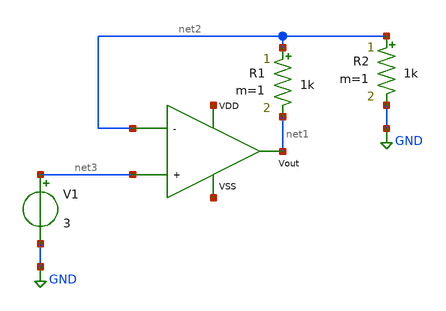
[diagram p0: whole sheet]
** sch_path: xschem/ota_miller/untitled.sch
**.subckt untitled
x1 net4 net1 net3 net2 net5 ota_n_in
V1 net3 GND 3
R1 net2 net1 1k m=1
R2 net2 GND 1k m=1
**.ends

* expanding   symbol:  ota_n_in.sym # of pins=5
** sym_path: xschem/ota_miller/ota_n_in.sym
** sch_path: xschem/ota_miller/ota_n_in.sch
.subckt ota_n_in VDD Vout + - VSS
*.opin Vout
*.ipin VSS
*.ipin VDD
*.ipin +
*.ipin -
XM1 net2 + net1 VSS nfet_03v3 L=0.28u W=0.22u nf=1 ad='int((nf+1)/2) * W/nf * 0.18u' as='int((nf+2)/2) * W/nf * 0.18u'
+ pd='2*int((nf+1)/2) * (W/nf + 0.18u)' ps='2*int((nf+2)/2) * (W/nf + 0.18u)' nrd='0.18u / W' nrs='0.18u / W'
+ sa=0 sb=0 sd=0 m=1 par=1
XM2 Vout - net1 VSS nfet_03v3 L=0.28u W=0.22u nf=1 ad='int((nf+1)/2) * W/nf * 0.18u' as='int((nf+2)/2) * W/nf * 0.18u'
+ pd='2*int((nf+1)/2) * (W/nf + 0.18u)' ps='2*int((nf+2)/2) * (W/nf + 0.18u)' nrd='0.18u / W' nrs='0.18u / W'
+ sa=0 sb=0 sd=0 m=1 par=1
XM3 VDD VDD net2 VSS nfet_03v3 L=0.28u W=0.22u nf=1 ad='int((nf+1)/2) * W/nf * 0.18u' as='int((nf+2)/2) * W/nf * 0.18u'
+ pd='2*int((nf+1)/2) * (W/nf + 0.18u)' ps='2*int((nf+2)/2) * (W/nf + 0.18u)' nrd='0.18u / W' nrs='0.18u / W'
+ sa=0 sb=0 sd=0 m=1 par=1
XM4 VDD VDD Vout VSS nfet_03v3 L=0.28u W=0.22u nf=1 ad='int((nf+1)/2) * W/nf * 0.18u' as='int((nf+2)/2) * W/nf * 0.18u'
+ pd='2*int((nf+1)/2) * (W/nf + 0.18u)' ps='2*int((nf+2)/2) * (W/nf + 0.18u)' nrd='0.18u / W' nrs='0.18u / W'
+ sa=0 sb=0 sd=0 m=1 par=1
XM5 net1 net3 VSS VSS nfet_03v3 L=0.28u W=0.22u nf=1 ad='int((nf+1)/2) * W/nf * 0.18u' as='int((nf+2)/2) * W/nf * 0.18u'
+ pd='2*int((nf+1)/2) * (W/nf + 0.18u)' ps='2*int((nf+2)/2) * (W/nf + 0.18u)' nrd='0.18u / W' nrs='0.18u / W'
+ sa=0 sb=0 sd=0 m=1 par=1
XM6 net3 net3 VSS VSS nfet_03v3 L=0.28u W=0.22u nf=1 ad='int((nf+1)/2) * W/nf * 0.18u' as='int((nf+2)/2) * W/nf * 0.18u'
+ pd='2*int((nf+1)/2) * (W/nf + 0.18u)' ps='2*int((nf+2)/2) * (W/nf + 0.18u)' nrd='0.18u / W' nrs='0.18u / W'
+ sa=0 sb=0 sd=0 m=1 par=1
I0 VDD net3 1m
.ends

.GLOBAL GND
.end
